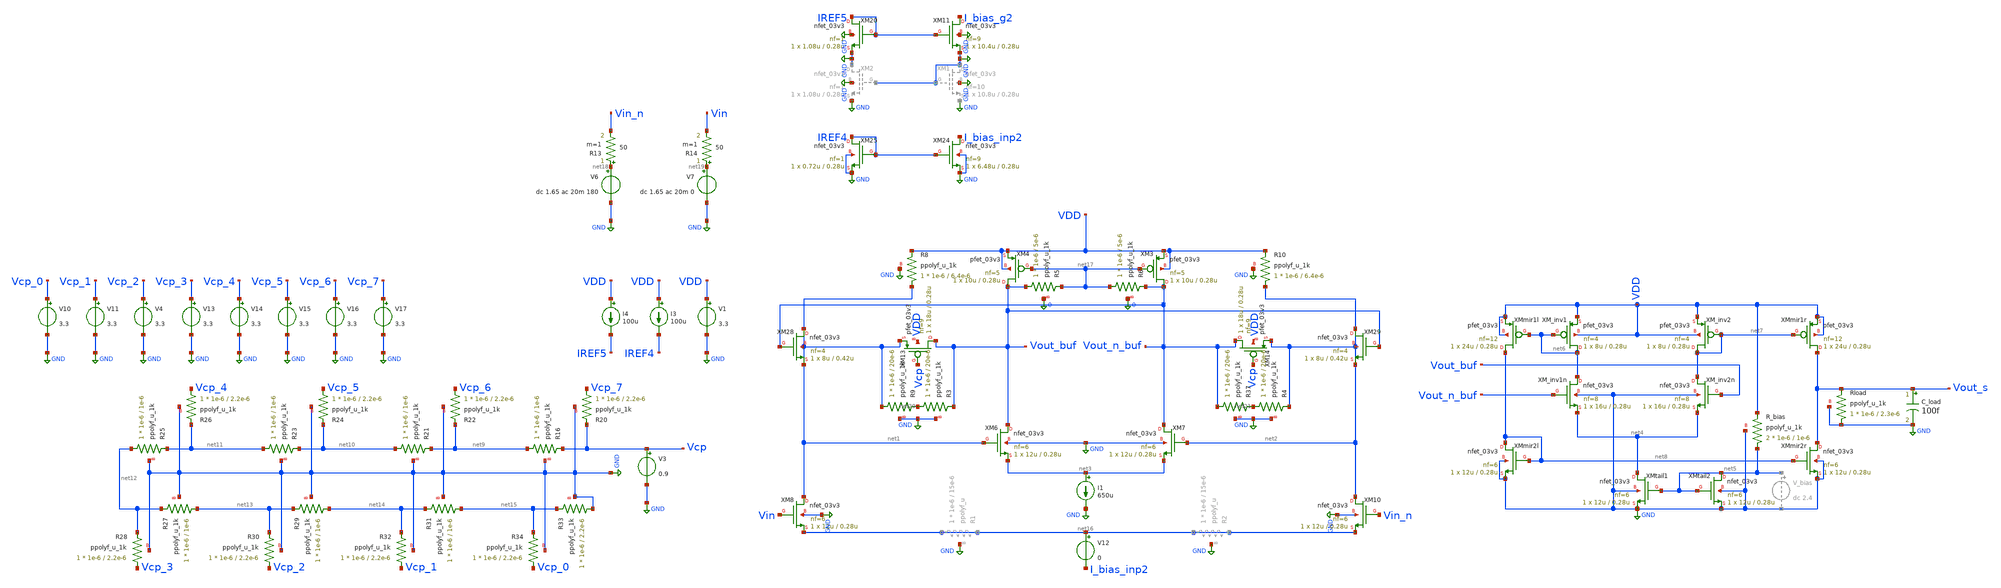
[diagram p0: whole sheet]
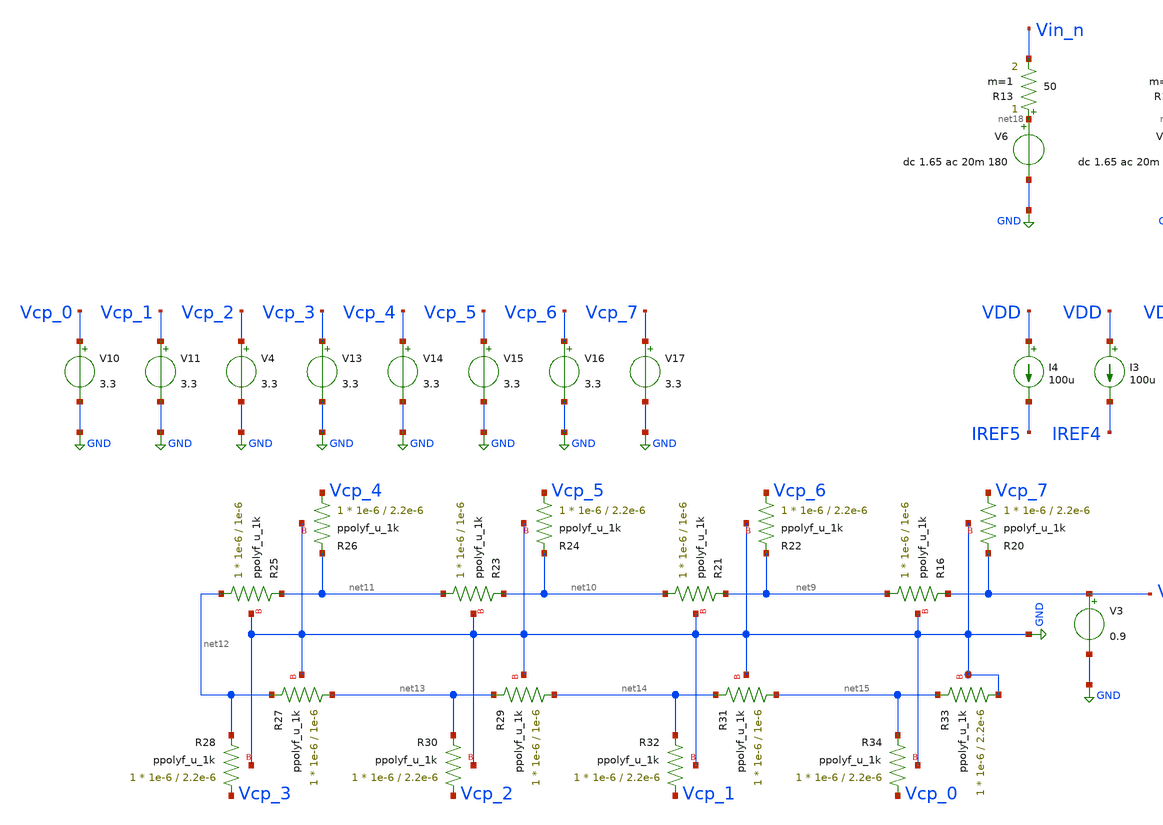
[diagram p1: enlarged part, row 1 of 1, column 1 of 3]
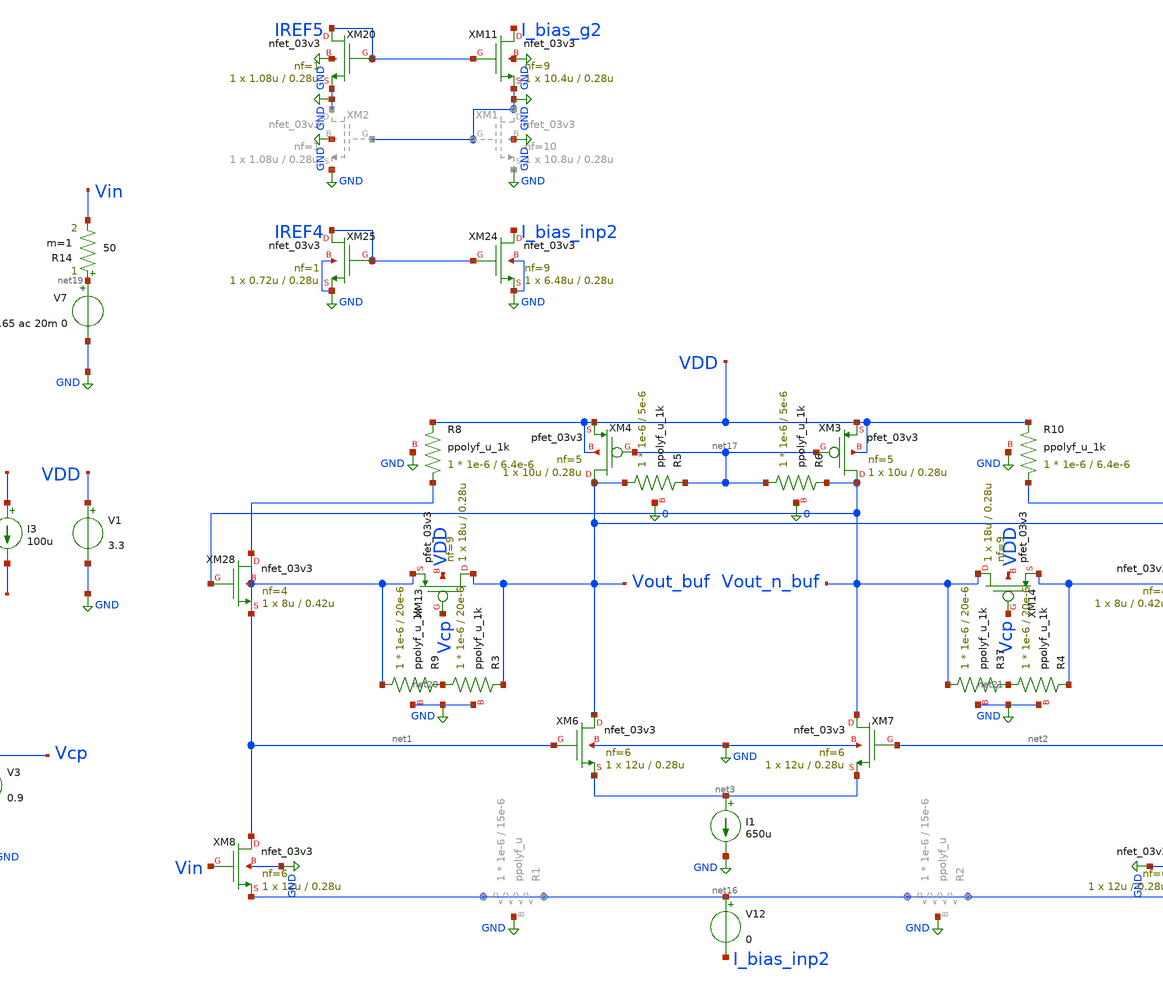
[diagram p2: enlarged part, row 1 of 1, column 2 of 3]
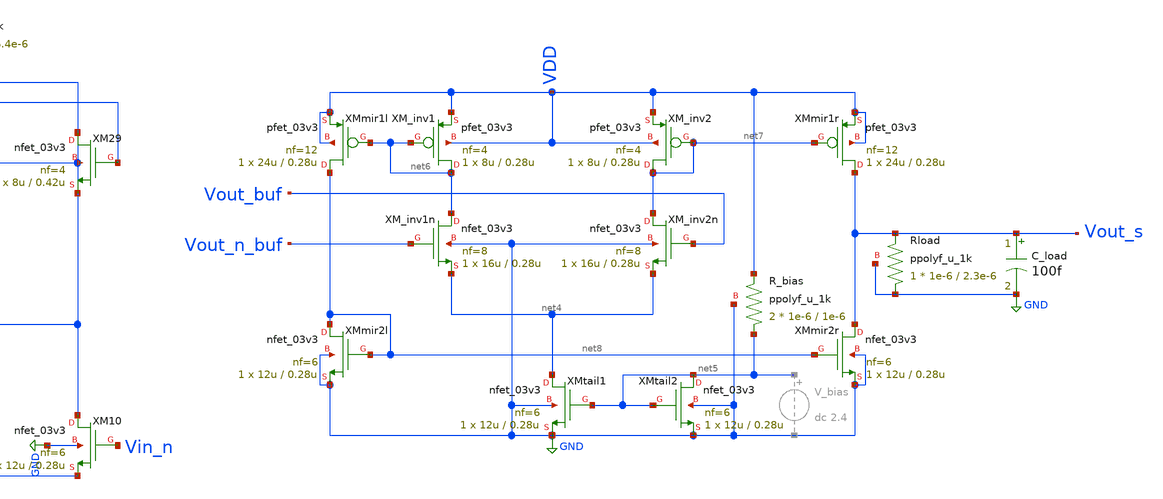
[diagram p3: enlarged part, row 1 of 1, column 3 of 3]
** sch_path: blocks/vga/vga.sch
**.subckt vga
V1 VDD GND 3.3
V6 net18 GND dc 1.65 ac 20m 180
XM6 Vout_buf net1 net3 GND nfet_03v3 L=0.28u W=12u nf=6 ad='int((nf+1)/2) * W/nf * 0.18u' as='int((nf+2)/2) * W/nf * 0.18u'
+ pd='2*int((nf+1)/2) * (W/nf + 0.18u)' ps='2*int((nf+2)/2) * (W/nf + 0.18u)' nrd='0.18u / W' nrs='0.18u / W'
+ sa=0 sb=0 sd=0 m=1
XM7 Vout_n_buf net2 net3 GND nfet_03v3 L=0.28u W=12u nf=6 ad='int((nf+1)/2) * W/nf * 0.18u' as='int((nf+2)/2) * W/nf * 0.18u'
+ pd='2*int((nf+1)/2) * (W/nf + 0.18u)' ps='2*int((nf+2)/2) * (W/nf + 0.18u)' nrd='0.18u / W' nrs='0.18u / W'
+ sa=0 sb=0 sd=0 m=1
XM8 net1 Vin net16 GND nfet_03v3 L=0.28u W=12u nf=6 ad='int((nf+1)/2) * W/nf * 0.18u' as='int((nf+2)/2) * W/nf * 0.18u'
+ pd='2*int((nf+1)/2) * (W/nf + 0.18u)' ps='2*int((nf+2)/2) * (W/nf + 0.18u)' nrd='0.18u / W' nrs='0.18u / W'
+ sa=0 sb=0 sd=0 m=1
XM10 net2 Vin_n net16 GND nfet_03v3 L=0.28u W=12u nf=6 ad='int((nf+1)/2) * W/nf * 0.18u' as='int((nf+2)/2) * W/nf * 0.18u'
+ pd='2*int((nf+1)/2) * (W/nf + 0.18u)' ps='2*int((nf+2)/2) * (W/nf + 0.18u)' nrd='0.18u / W' nrs='0.18u / W'
+ sa=0 sb=0 sd=0 m=1
V7 net19 GND dc 1.65 ac 20m 0
R14 net19 Vin 50 m=1
R13 net18 Vin_n 50 m=1
XM28 net1 Vout_n_buf net1 net1 nfet_03v3 L=0.42u W=8u nf=4 ad='int((nf+1)/2) * W/nf * 0.18u' as='int((nf+2)/2) * W/nf * 0.18u'
+ pd='2*int((nf+1)/2) * (W/nf + 0.18u)' ps='2*int((nf+2)/2) * (W/nf + 0.18u)' nrd='0.18u / W' nrs='0.18u / W'
+ sa=0 sb=0 sd=0 m=1
XM29 net2 Vout_buf net2 net2 nfet_03v3 L=0.42u W=8u nf=4 ad='int((nf+1)/2) * W/nf * 0.18u' as='int((nf+2)/2) * W/nf * 0.18u'
+ pd='2*int((nf+1)/2) * (W/nf + 0.18u)' ps='2*int((nf+2)/2) * (W/nf + 0.18u)' nrd='0.18u / W' nrs='0.18u / W'
+ sa=0 sb=0 sd=0 m=1
XM_inv1 net6 net6 VDD VDD pfet_03v3 L=0.28u W=8u nf=4 ad='int((nf+1)/2) * W/nf * 0.18u' as='int((nf+2)/2) * W/nf * 0.18u'
+ pd='2*int((nf+1)/2) * (W/nf + 0.18u)' ps='2*int((nf+2)/2) * (W/nf + 0.18u)' nrd='0.18u / W' nrs='0.18u / W'
+ sa=0 sb=0 sd=0 m=1
XM_inv1n net6 Vout_n_buf net4 GND nfet_03v3 L=0.28u W=16u nf=8 ad='int((nf+1)/2) * W/nf * 0.18u' as='int((nf+2)/2) * W/nf * 0.18u'
+ pd='2*int((nf+1)/2) * (W/nf + 0.18u)' ps='2*int((nf+2)/2) * (W/nf + 0.18u)' nrd='0.18u / W' nrs='0.18u / W'
+ sa=0 sb=0 sd=0 m=1
XM_inv2 net7 net7 VDD VDD pfet_03v3 L=0.28u W=8u nf=4 ad='int((nf+1)/2) * W/nf * 0.18u' as='int((nf+2)/2) * W/nf * 0.18u'
+ pd='2*int((nf+1)/2) * (W/nf + 0.18u)' ps='2*int((nf+2)/2) * (W/nf + 0.18u)' nrd='0.18u / W' nrs='0.18u / W'
+ sa=0 sb=0 sd=0 m=1
XM_inv2n net7 Vout_buf net4 GND nfet_03v3 L=0.28u W=16u nf=8 ad='int((nf+1)/2) * W/nf * 0.18u' as='int((nf+2)/2) * W/nf * 0.18u'
+ pd='2*int((nf+1)/2) * (W/nf + 0.18u)' ps='2*int((nf+2)/2) * (W/nf + 0.18u)' nrd='0.18u / W' nrs='0.18u / W'
+ sa=0 sb=0 sd=0 m=1
XMtail1 net4 net5 GND GND nfet_03v3 L=0.28u W=12u nf=6 ad='int((nf+1)/2) * W/nf * 0.18u' as='int((nf+2)/2) * W/nf * 0.18u'
+ pd='2*int((nf+1)/2) * (W/nf + 0.18u)' ps='2*int((nf+2)/2) * (W/nf + 0.18u)' nrd='0.18u / W' nrs='0.18u / W'
+ sa=0 sb=0 sd=0 m=1
XMtail2 net5 net5 GND GND nfet_03v3 L=0.28u W=12u nf=6 ad='int((nf+1)/2) * W/nf * 0.18u' as='int((nf+2)/2) * W/nf * 0.18u'
+ pd='2*int((nf+1)/2) * (W/nf + 0.18u)' ps='2*int((nf+2)/2) * (W/nf + 0.18u)' nrd='0.18u / W' nrs='0.18u / W'
+ sa=0 sb=0 sd=0 m=1
XMmir1l net8 net6 VDD VDD pfet_03v3 L=0.28u W=24u nf=12 ad='int((nf+1)/2) * W/nf * 0.18u' as='int((nf+2)/2) * W/nf * 0.18u'
+ pd='2*int((nf+1)/2) * (W/nf + 0.18u)' ps='2*int((nf+2)/2) * (W/nf + 0.18u)' nrd='0.18u / W' nrs='0.18u / W'
+ sa=0 sb=0 sd=0 m=1
XMmir1r Vout_s net7 VDD VDD pfet_03v3 L=0.28u W=24u nf=12 ad='int((nf+1)/2) * W/nf * 0.18u' as='int((nf+2)/2) * W/nf * 0.18u'
+ pd='2*int((nf+1)/2) * (W/nf + 0.18u)' ps='2*int((nf+2)/2) * (W/nf + 0.18u)' nrd='0.18u / W' nrs='0.18u / W'
+ sa=0 sb=0 sd=0 m=1
XMmir2l net8 net8 GND GND nfet_03v3 L=0.28u W=12u nf=6 ad='int((nf+1)/2) * W/nf * 0.18u' as='int((nf+2)/2) * W/nf * 0.18u'
+ pd='2*int((nf+1)/2) * (W/nf + 0.18u)' ps='2*int((nf+2)/2) * (W/nf + 0.18u)' nrd='0.18u / W' nrs='0.18u / W'
+ sa=0 sb=0 sd=0 m=1
XMmir2r Vout_s net8 GND GND nfet_03v3 L=0.28u W=12u nf=6 ad='int((nf+1)/2) * W/nf * 0.18u' as='int((nf+2)/2) * W/nf * 0.18u'
+ pd='2*int((nf+1)/2) * (W/nf + 0.18u)' ps='2*int((nf+2)/2) * (W/nf + 0.18u)' nrd='0.18u / W' nrs='0.18u / W'
+ sa=0 sb=0 sd=0 m=1
XR_bias net5 VDD GND ppolyf_u_1k r_width=1e-6 r_length=1e-6 m=2
C_load Vout_s GND 100f m=1
XR16 net9 Vcp GND ppolyf_u_1k r_width=1e-6 r_length=1e-6 m=1
XR20 Vcp_7 Vcp GND ppolyf_u_1k r_width=1e-6 r_length=2.2e-6 m=1
XR21 net10 net9 GND ppolyf_u_1k r_width=1e-6 r_length=1e-6 m=1
XR22 Vcp_6 net9 GND ppolyf_u_1k r_width=1e-6 r_length=2.2e-6 m=1
XR23 net11 net10 GND ppolyf_u_1k r_width=1e-6 r_length=1e-6 m=1
XR24 Vcp_5 net10 GND ppolyf_u_1k r_width=1e-6 r_length=2.2e-6 m=1
XR25 net12 net11 GND ppolyf_u_1k r_width=1e-6 r_length=1e-6 m=1
XR26 Vcp_4 net11 GND ppolyf_u_1k r_width=1e-6 r_length=2.2e-6 m=1
XR27 net13 net12 GND ppolyf_u_1k r_width=1e-6 r_length=1e-6 m=1
XR28 Vcp_3 net12 GND ppolyf_u_1k r_width=1e-6 r_length=2.2e-6 m=1
XR29 net14 net13 GND ppolyf_u_1k r_width=1e-6 r_length=1e-6 m=1
XR30 Vcp_2 net13 GND ppolyf_u_1k r_width=1e-6 r_length=2.2e-6 m=1
XR31 net15 net14 GND ppolyf_u_1k r_width=1e-6 r_length=1e-6 m=1
XR32 Vcp_1 net14 GND ppolyf_u_1k r_width=1e-6 r_length=2.2e-6 m=1
XR33 GND net15 GND ppolyf_u_1k r_width=1e-6 r_length=2.2e-6 m=1
XR34 Vcp_0 net15 GND ppolyf_u_1k r_width=1e-6 r_length=2.2e-6 m=1
V10 Vcp_0 GND 3.3
V11 Vcp_1 GND 3.3
V4 Vcp_2 GND 3.3
V13 Vcp_3 GND 3.3
V14 Vcp_4 GND 3.3
V15 Vcp_5 GND 3.3
V16 Vcp_6 GND 3.3
V17 Vcp_7 GND 3.3
V3 Vcp GND 0.9
XM13 Vout_buf Vcp net1 VDD pfet_03v3 L=0.28u W=18u nf=9 ad='int((nf+1)/2) * W/nf * 0.18u' as='int((nf+2)/2) * W/nf * 0.18u'
+ pd='2*int((nf+1)/2) * (W/nf + 0.18u)' ps='2*int((nf+2)/2) * (W/nf + 0.18u)' nrd='0.18u / W' nrs='0.18u / W'
+ sa=0 sb=0 sd=0 m=1
XR9 net1 net20 GND ppolyf_u_1k r_width=1e-6 r_length=20e-6 m=1
XM14 Vout_n_buf Vcp net2 VDD pfet_03v3 L=0.28u W=18u nf=9 ad='int((nf+1)/2) * W/nf * 0.18u' as='int((nf+2)/2) * W/nf * 0.18u'
+ pd='2*int((nf+1)/2) * (W/nf + 0.18u)' ps='2*int((nf+2)/2) * (W/nf + 0.18u)' nrd='0.18u / W' nrs='0.18u / W'
+ sa=0 sb=0 sd=0 m=1
XR37 Vout_n_buf net21 GND ppolyf_u_1k r_width=1e-6 r_length=20e-6 m=1
XRload GND Vout_s GND ppolyf_u_1k r_width=1e-6 r_length=2.3e-6 m=1
XR8 net1 VDD GND ppolyf_u_1k r_width=1e-6 r_length=6.4e-6 m=1
XR10 net2 VDD GND ppolyf_u_1k r_width=1e-6 r_length=6.4e-6 m=1
XM11 I_bias_g2 IREF5 GND GND nfet_03v3 L=0.28u W=10.4u nf=9 ad='int((nf+1)/2) * W/nf * 0.18u' as='int((nf+2)/2) * W/nf * 0.18u'
+ pd='2*int((nf+1)/2) * (W/nf + 0.18u)' ps='2*int((nf+2)/2) * (W/nf + 0.18u)' nrd='0.18u / W' nrs='0.18u / W'
+ sa=0 sb=0 sd=0 m=1
XM20 IREF5 IREF5 GND GND nfet_03v3 L=0.28u W=1.08u nf=1 ad='int((nf+1)/2) * W/nf * 0.18u' as='int((nf+2)/2) * W/nf * 0.18u'
+ pd='2*int((nf+1)/2) * (W/nf + 0.18u)' ps='2*int((nf+2)/2) * (W/nf + 0.18u)' nrd='0.18u / W' nrs='0.18u / W'
+ sa=0 sb=0 sd=0 m=1
I3 VDD IREF4 100u
XM24 I_bias_inp2 IREF4 GND GND nfet_03v3 L=0.28u W=6.48u nf=9 ad='int((nf+1)/2) * W/nf * 0.18u' as='int((nf+2)/2) * W/nf * 0.18u'
+ pd='2*int((nf+1)/2) * (W/nf + 0.18u)' ps='2*int((nf+2)/2) * (W/nf + 0.18u)' nrd='0.18u / W' nrs='0.18u / W'
+ sa=0 sb=0 sd=0 m=1
XM25 IREF4 IREF4 GND GND nfet_03v3 L=0.28u W=0.72u nf=1 ad='int((nf+1)/2) * W/nf * 0.18u' as='int((nf+2)/2) * W/nf * 0.18u'
+ pd='2*int((nf+1)/2) * (W/nf + 0.18u)' ps='2*int((nf+2)/2) * (W/nf + 0.18u)' nrd='0.18u / W' nrs='0.18u / W'
+ sa=0 sb=0 sd=0 m=1
I4 VDD IREF5 100u
V12 net16 I_bias_inp2 0
XR3 net20 Vout_buf GND ppolyf_u_1k r_width=1e-6 r_length=20e-6 m=1
XR4 net21 net2 GND ppolyf_u_1k r_width=1e-6 r_length=20e-6 m=1
I1 net3 GND 650u
XM3 Vout_n_buf net17 VDD VDD pfet_03v3 L=0.28u W=10u nf=5 ad='int((nf+1)/2) * W/nf * 0.18u' as='int((nf+2)/2) * W/nf * 0.18u'
+ pd='2*int((nf+1)/2) * (W/nf + 0.18u)' ps='2*int((nf+2)/2) * (W/nf + 0.18u)' nrd='0.18u / W' nrs='0.18u / W'
+ sa=0 sb=0 sd=0 m=1
XM4 Vout_buf net17 VDD VDD pfet_03v3 L=0.28u W=10u nf=5 ad='int((nf+1)/2) * W/nf * 0.18u' as='int((nf+2)/2) * W/nf * 0.18u'
+ pd='2*int((nf+1)/2) * (W/nf + 0.18u)' ps='2*int((nf+2)/2) * (W/nf + 0.18u)' nrd='0.18u / W' nrs='0.18u / W'
+ sa=0 sb=0 sd=0 m=1
XR5 Vout_buf net17 0 ppolyf_u_1k r_width=1e-6 r_length=5e-6 m=1
XR6 net17 Vout_n_buf 0 ppolyf_u_1k r_width=1e-6 r_length=5e-6 m=1
**** begin user architecture code


.include /foss/pdks/gf180mcuD/libs.tech/ngspice/design.ngspice
.lib /foss/pdks/gf180mcuD/libs.tech/ngspice/sm141064.ngspice typical
.lib /foss/pdks/gf180mcuD/libs.tech/ngspice/sm141064.ngspice bjt_typical
.lib /foss/pdks/gf180mcuD/libs.tech/ngspice/sm141064.ngspice diode_typical
.lib /foss/pdks/gf180mcuD/libs.tech/ngspice/sm141064.ngspice res_typical
.lib /foss/pdks/gf180mcuD/libs.tech/ngspice/sm141064.ngspice mimcap_typical
.lib /foss/pdks/gf180mcuD/libs.tech/ngspice/sm141064.ngspice moscap_typical
.option method=gear

.control
set temp = 25
  * 1. Setup the sweep parameters
  let v_start = 0
  let v_stop = 3.3
  let v_points = 66
  let v_delta = (v_stop - v_start) / v_points

  * 2. Initialize vectors to store results
  let gain_db_20 = unitvec(v_points + 1)
  let gain_db_1200 = unitvec(v_points + 1)
  let vcp_axis = unitvec(v_points + 1)

  let i = 0
  while i <= v_points
    let v_current = v_start + (i * v_delta)
    alter v3 = v_current   ; Adjust the Vcp source DC value

    * 3. Run AC analysis ONLY at 600MHz to maximize speed
    ac lin 3 0.02G 1.2G

    * 4. Calculate Differential Gain in dB
    * Formula: 20 * log10(|Vout_diff| / |Vin_diff|)
    * let vout_mag = mag(v(vout_buf) - v(vout_n_buf))
    let vout_mag = mag(v(vout_s))
    let vin_mag = mag(v(vin) - v(vin_n))
    let g_val = 20 * log10(vout_mag / vin_mag)

    * 5. Save results to vectors
    let gain_db_20[i] = g_val[1]
    let gain_db_1200[i] = g_val[2]
    let vcp_axis[i] = v_current
    let i = i + 1
    *print mag(v(vout) - v(vout_n))
    *print i(v1)
  end

  * 6. Plot the Gain vs Control Voltage
  plot gain_db_20 gain_db_1200 vs vcp_axis title 'VGA Gain at 20MHz, 1.2GHz vs Vcp, 100fF load' xlabel
+ 'Vcp (V)' ylabel 'Gain (dB)'
.endc


**** end user architecture code
**.ends
.GLOBAL GND
.end
